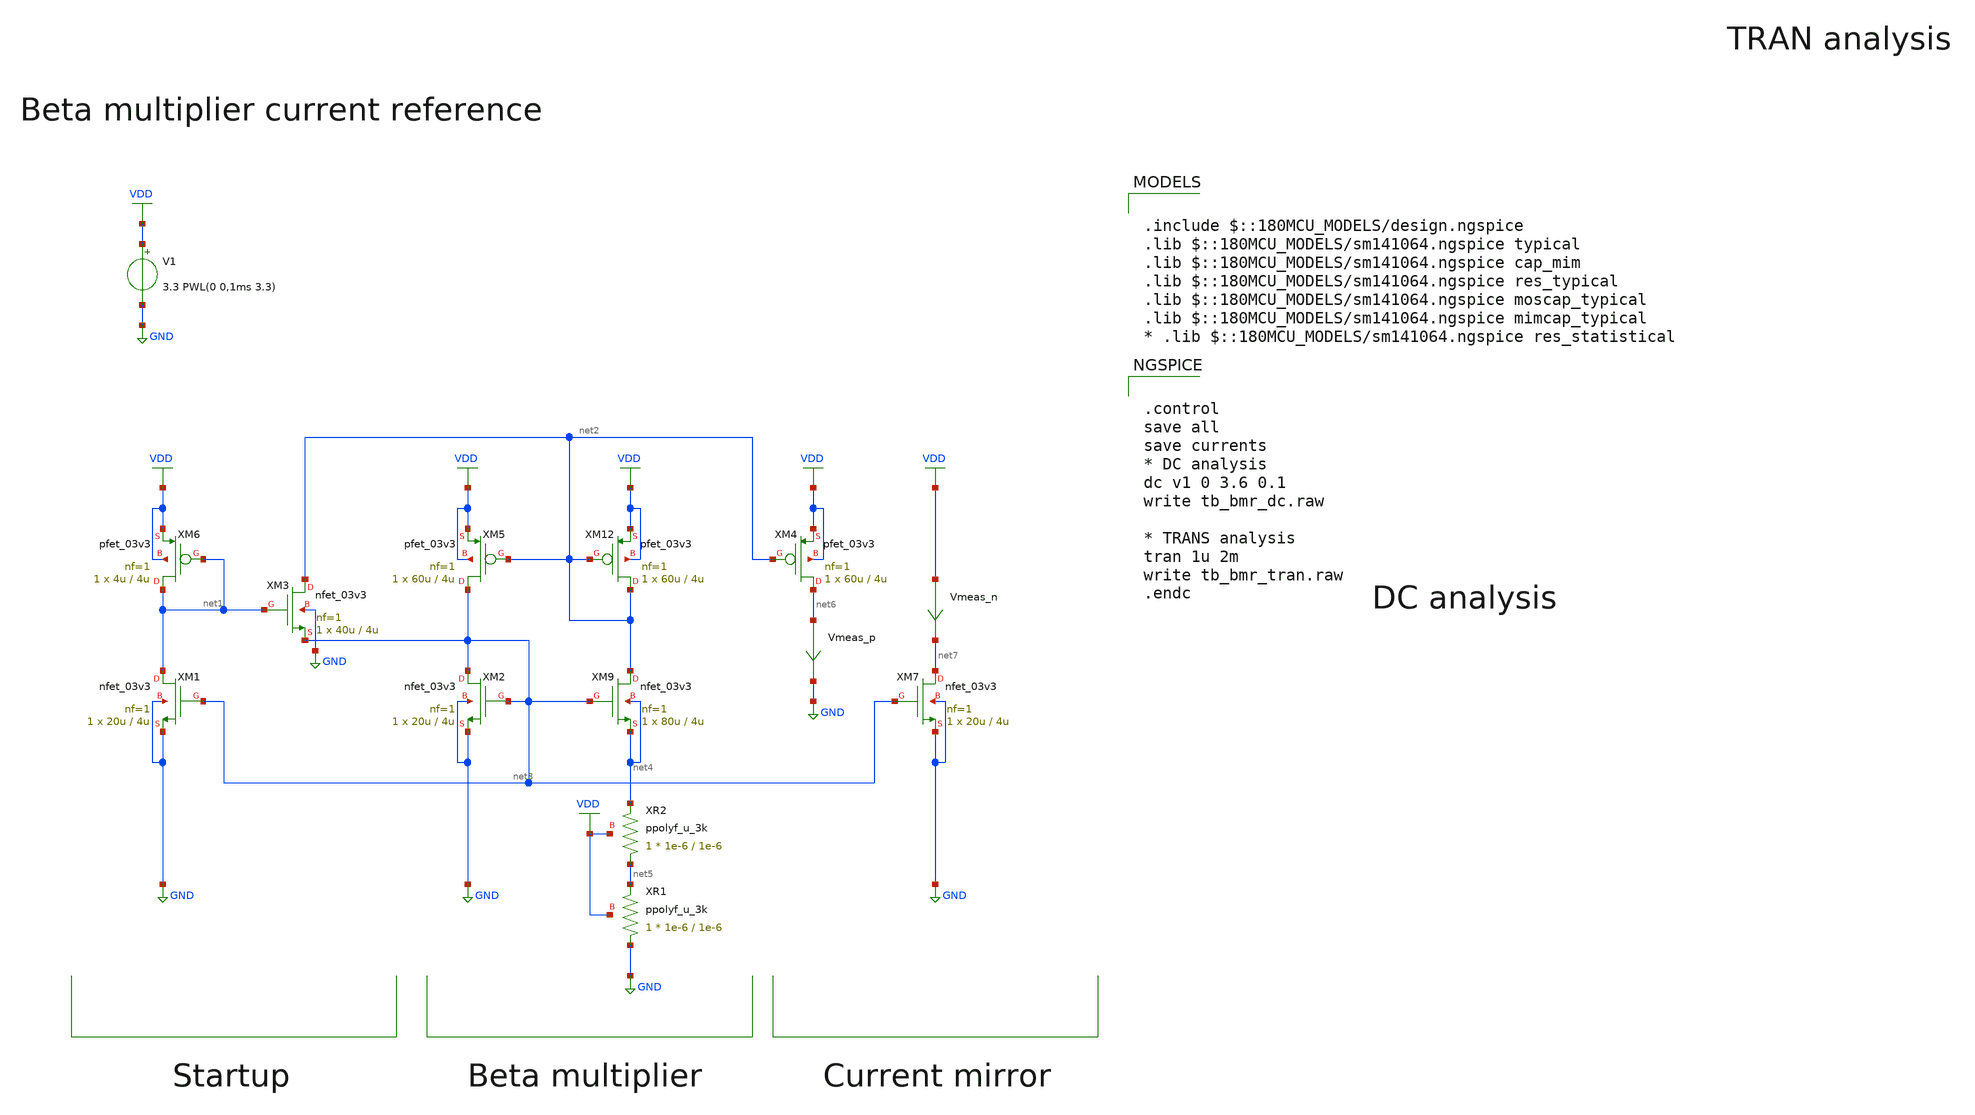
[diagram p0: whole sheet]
** sch_path: designs/libs/tb_analog/tb_bmr/tb_bmr_dc.sch
* Copyright 2022 GlobalFoundries PDK Authors
* Licensed under the Apache License, Version 2.0 (the "License");
* you may not use this file except in compliance with the License.
* You may obtain a copy of the License at
* https://www.apache.org/licenses/LICENSE-2.0
* Unless required by applicable law or agreed to in writing, software
* distributed under the License is distributed on an "AS IS" BASIS,
* WITHOUT WARRANTIES OR CONDITIONS OF ANY KIND, either express or implied.
* See the License for the specific language governing permissions and
* limitations under the License.
**.subckt tb_bmr_dc
V1 VDD GND 3.3 PWL(0 0,1ms 3.3)
XM3 net2 net1 net3 GND nfet_03v3 L=4u W=40u nf=1 ad='int((nf+1)/2) * W/nf * 0.18u' as='int((nf+2)/2) * W/nf * 0.18u'
+ pd='2*int((nf+1)/2) * (W/nf + 0.18u)' ps='2*int((nf+2)/2) * (W/nf + 0.18u)' nrd='0.18u / W' nrs='0.18u / W'
+ sa=0 sb=0 sd=0 m=1
XM5 net3 net2 VDD VDD pfet_03v3 L=4u W=60u nf=1 ad='int((nf+1)/2) * W/nf * 0.18u' as='int((nf+2)/2) * W/nf * 0.18u'
+ pd='2*int((nf+1)/2) * (W/nf + 0.18u)' ps='2*int((nf+2)/2) * (W/nf + 0.18u)' nrd='0.18u / W' nrs='0.18u / W'
+ sa=0 sb=0 sd=0 m=1
XM6 net1 net1 VDD VDD pfet_03v3 L=4u W=4u nf=1 ad='int((nf+1)/2) * W/nf * 0.18u' as='int((nf+2)/2) * W/nf * 0.18u'
+ pd='2*int((nf+1)/2) * (W/nf + 0.18u)' ps='2*int((nf+2)/2) * (W/nf + 0.18u)' nrd='0.18u / W' nrs='0.18u / W'
+ sa=0 sb=0 sd=0 m=1
XM9 net2 net3 net4 net4 nfet_03v3 L=4u W=80u nf=1 ad='int((nf+1)/2) * W/nf * 0.18u' as='int((nf+2)/2) * W/nf * 0.18u'
+ pd='2*int((nf+1)/2) * (W/nf + 0.18u)' ps='2*int((nf+2)/2) * (W/nf + 0.18u)' nrd='0.18u / W' nrs='0.18u / W'
+ sa=0 sb=0 sd=0 m=1
XM12 net2 net2 VDD VDD pfet_03v3 L=4u W=60u nf=1 ad='int((nf+1)/2) * W/nf * 0.18u' as='int((nf+2)/2) * W/nf * 0.18u'
+ pd='2*int((nf+1)/2) * (W/nf + 0.18u)' ps='2*int((nf+2)/2) * (W/nf + 0.18u)' nrd='0.18u / W' nrs='0.18u / W'
+ sa=0 sb=0 sd=0 m=1
XM1 net1 net3 GND GND nfet_03v3 L=4u W=20u nf=1 ad='int((nf+1)/2) * W/nf * 0.18u' as='int((nf+2)/2) * W/nf * 0.18u'
+ pd='2*int((nf+1)/2) * (W/nf + 0.18u)' ps='2*int((nf+2)/2) * (W/nf + 0.18u)' nrd='0.18u / W' nrs='0.18u / W'
+ sa=0 sb=0 sd=0 m=1
XM2 net3 net3 GND GND nfet_03v3 L=4u W=20u nf=1 ad='int((nf+1)/2) * W/nf * 0.18u' as='int((nf+2)/2) * W/nf * 0.18u'
+ pd='2*int((nf+1)/2) * (W/nf + 0.18u)' ps='2*int((nf+2)/2) * (W/nf + 0.18u)' nrd='0.18u / W' nrs='0.18u / W'
+ sa=0 sb=0 sd=0 m=1
XR2 net5 net4 VDD ppolyf_u_3k r_width=1e-6 r_length=1e-6 m=1
XM4 net6 net2 VDD VDD pfet_03v3 L=4u W=60u nf=1 ad='int((nf+1)/2) * W/nf * 0.18u' as='int((nf+2)/2) * W/nf * 0.18u'
+ pd='2*int((nf+1)/2) * (W/nf + 0.18u)' ps='2*int((nf+2)/2) * (W/nf + 0.18u)' nrd='0.18u / W' nrs='0.18u / W'
+ sa=0 sb=0 sd=0 m=1
Vmeas_p net6 GND 0
.save i(vmeas_p)
XM7 net7 net3 GND GND nfet_03v3 L=4u W=20u nf=1 ad='int((nf+1)/2) * W/nf * 0.18u' as='int((nf+2)/2) * W/nf * 0.18u'
+ pd='2*int((nf+1)/2) * (W/nf + 0.18u)' ps='2*int((nf+2)/2) * (W/nf + 0.18u)' nrd='0.18u / W' nrs='0.18u / W'
+ sa=0 sb=0 sd=0 m=1
Vmeas_n VDD net7 0
.save i(vmeas_n)
XR1 GND net5 VDD ppolyf_u_3k r_width=1e-6 r_length=1e-6 m=1
**** begin user architecture code


.control
save all
save currents
* DC analysis
dc v1 0 3.6 0.1
write tb_bmr_dc.raw

* TRANS analysis
tran 1u 2m
write tb_bmr_tran.raw
.endc



.include $::180MCU_MODELS/design.ngspice
.lib $::180MCU_MODELS/sm141064.ngspice typical
.lib $::180MCU_MODELS/sm141064.ngspice cap_mim
.lib $::180MCU_MODELS/sm141064.ngspice res_typical
.lib $::180MCU_MODELS/sm141064.ngspice moscap_typical
.lib $::180MCU_MODELS/sm141064.ngspice mimcap_typical
* .lib $::180MCU_MODELS/sm141064.ngspice res_statistical

**** end user architecture code
**.ends
.GLOBAL GND
.GLOBAL VDD
.end
